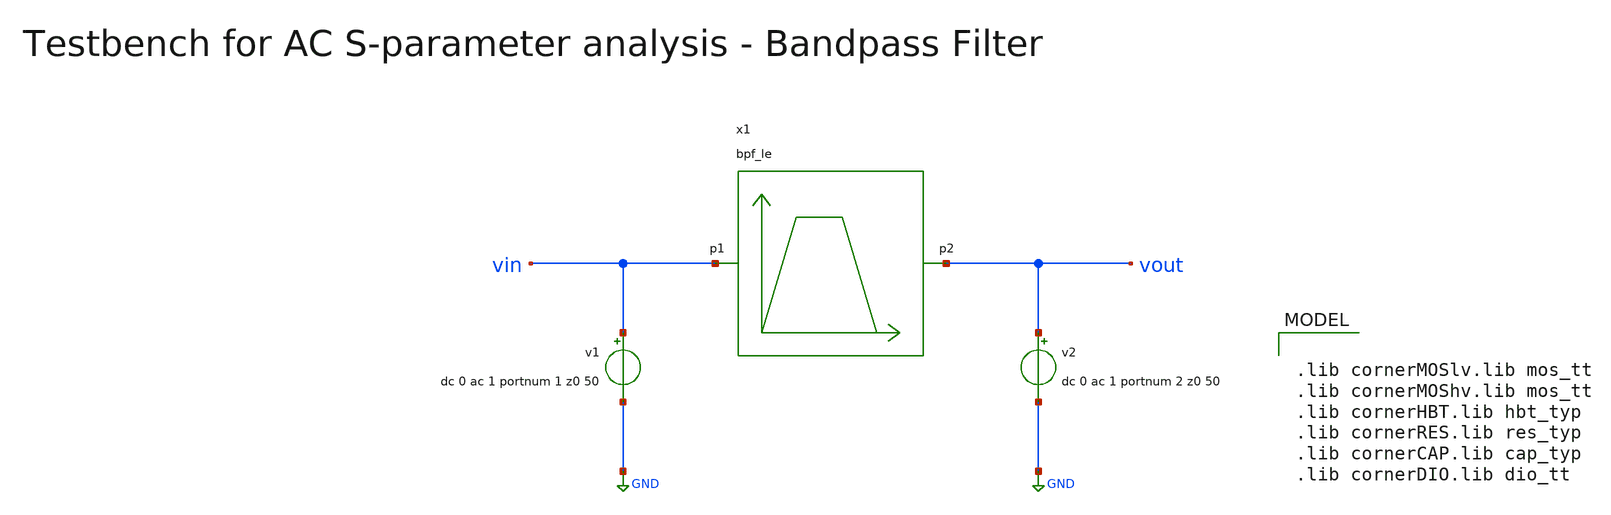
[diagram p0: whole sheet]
** sch_path: testbenches/xschem/bpf_le_tb_acsp_ngspice.sch
**.subckt bpf_le_tb_acsp_ngspice
v1 vin GND dc 0 ac 1 portnum 1 z0 50
v2 vout GND dc 0 ac 1 portnum 2 z0 50
x1 vin vout bpf_le
**** begin user architecture code


.include ../../../netlist/spice/bpf_le.spice
.param temp=27
.options savecurrents klu method=gear reltol=1e-3 abstol=1e-15 gmin=1e-15
.control

save all

set wr_vecnames
set wr_singlescale

* User Constants
let f_min = 120.0e9
let f_max = 200.0e9
let f0 = 160.0e9

* Operating Point Analysis
op
remzerovec
write @schname\.raw
set appendwrite

* AC S-Parameter Analysis
sp lin 1001 $&const.f_min $&const.f_max
remzerovec
write @schname\.raw
set appendwrite

* Calculating S-Parameters
let s11_dB = db(s_1_1)
let s21_dB = db(S_2_1)
let s12_dB = db(S_1_2)
let s22_dB = db(S_2_2)

let s11_deg = cph(S_1_1) * 180/pi
let s21_deg = cph(S_2_1) * 180/pi
let s12_deg = cph(S_1_2) * 180/pi
let s22_deg = cph(S_2_2) * 180/pi

* Plotting
plot s11_dB s22_dB
plot s11_deg s22_deg
plot s12_dB s21_dB
plot s12_deg s21_deg

* Write Data
unset appendwrite
set wr_vecnames
set wr_singlescale
wrdata ../../../sim_data/@schname\.txt  s11_dB s22_dB s12_dB s21_dB  s11_deg s22_deg s12_deg s21_deg

*quit
.endc



.lib cornerMOSlv.lib mos_tt
.lib cornerMOShv.lib mos_tt
.lib cornerHBT.lib hbt_typ
.lib cornerRES.lib res_typ
.lib cornerCAP.lib cap_typ
.lib cornerDIO.lib dio_tt

**** end user architecture code
**.ends
.GLOBAL GND
.end
